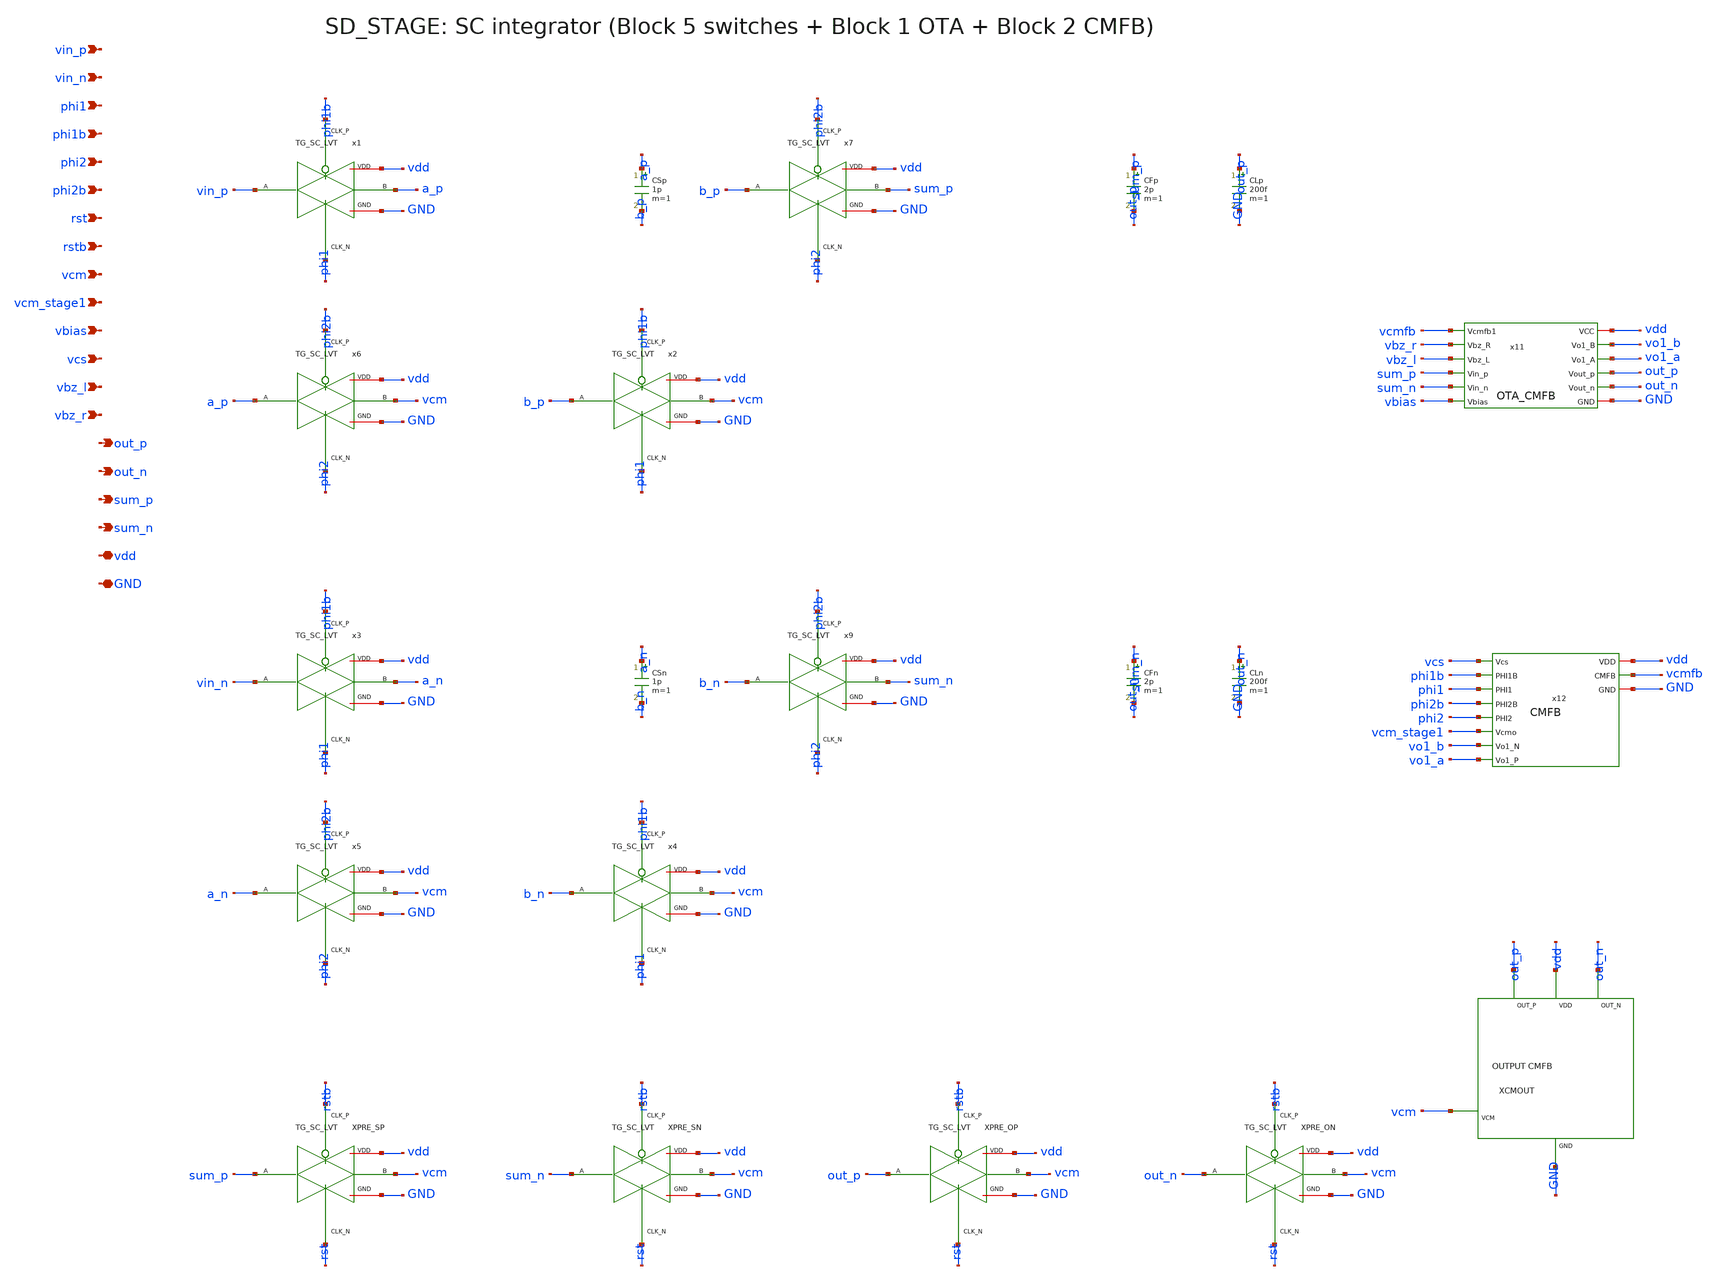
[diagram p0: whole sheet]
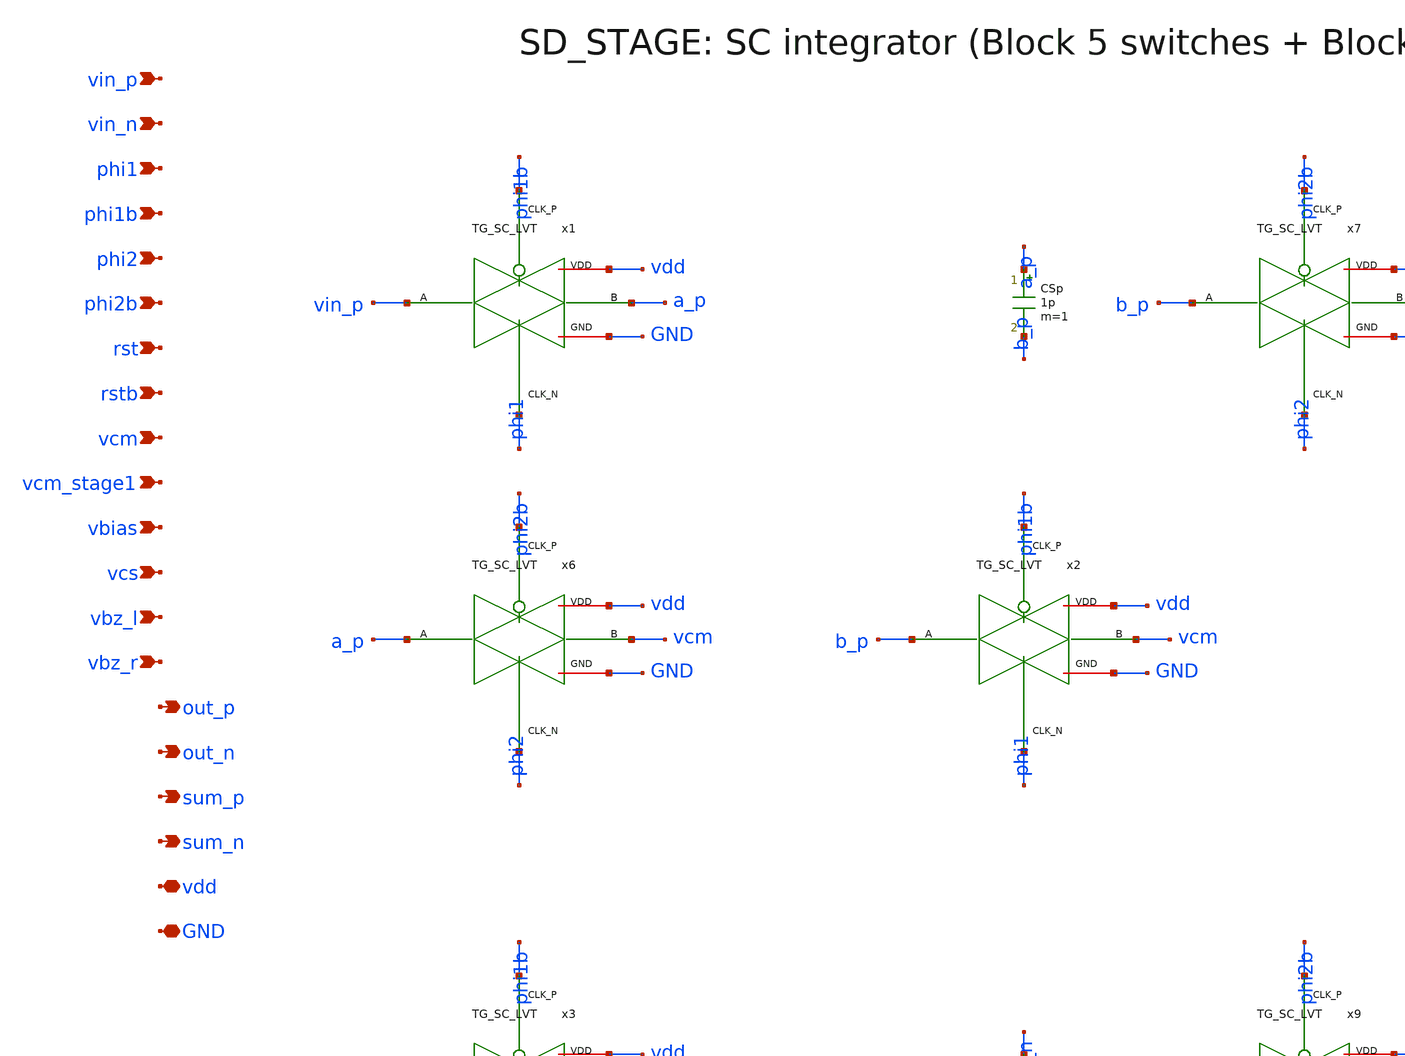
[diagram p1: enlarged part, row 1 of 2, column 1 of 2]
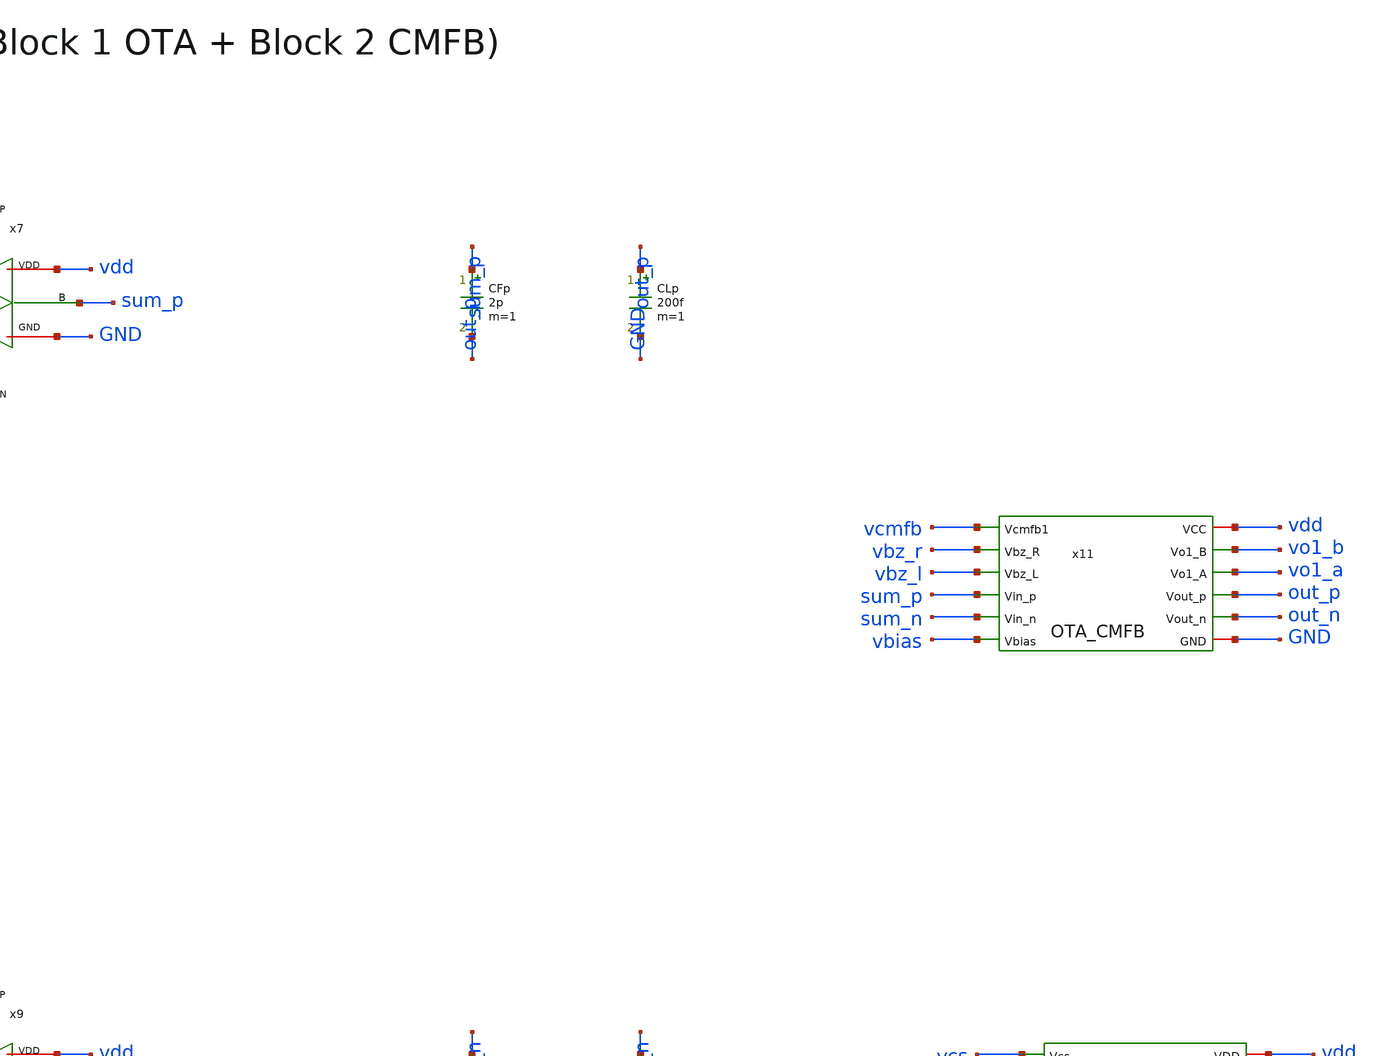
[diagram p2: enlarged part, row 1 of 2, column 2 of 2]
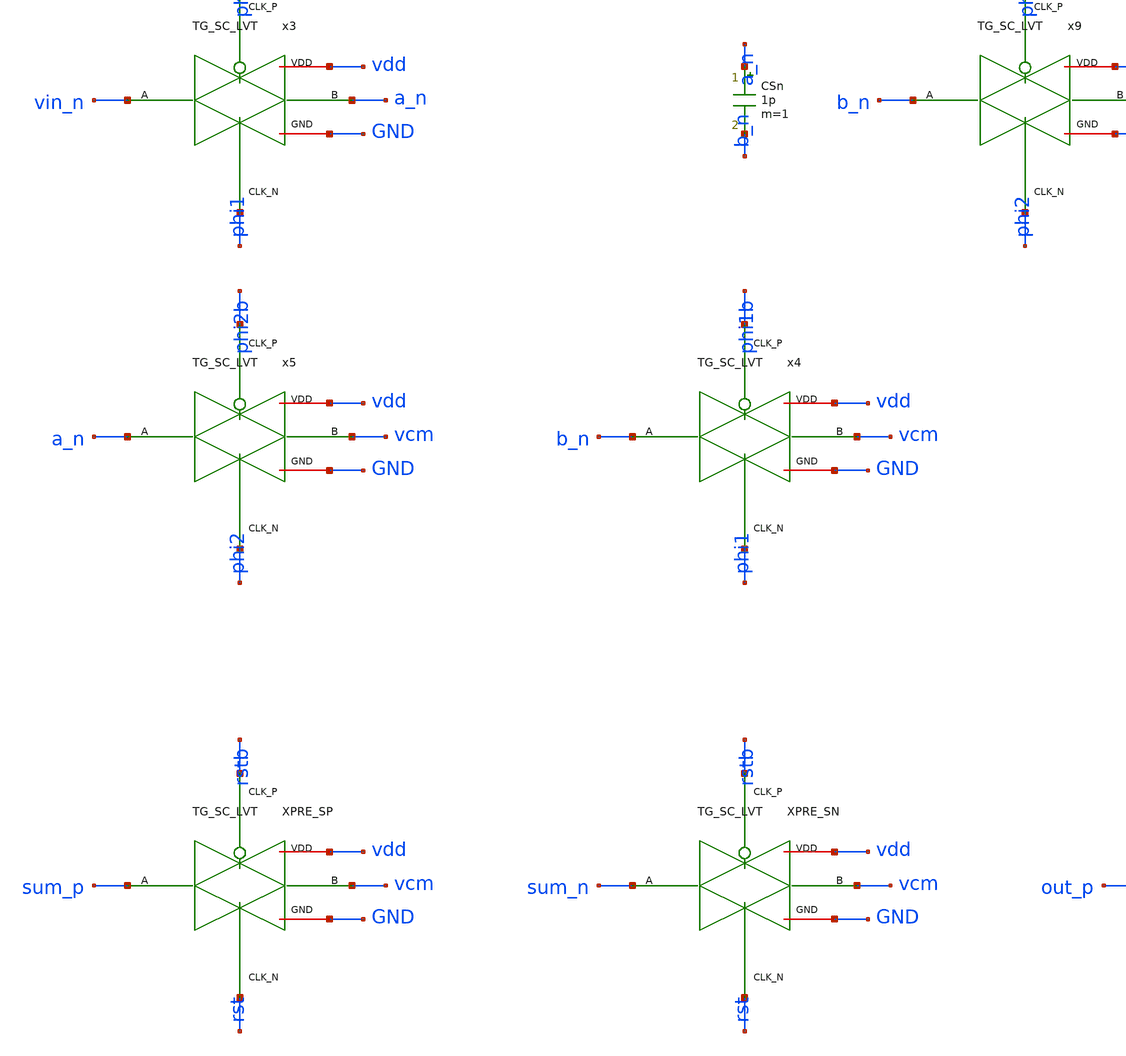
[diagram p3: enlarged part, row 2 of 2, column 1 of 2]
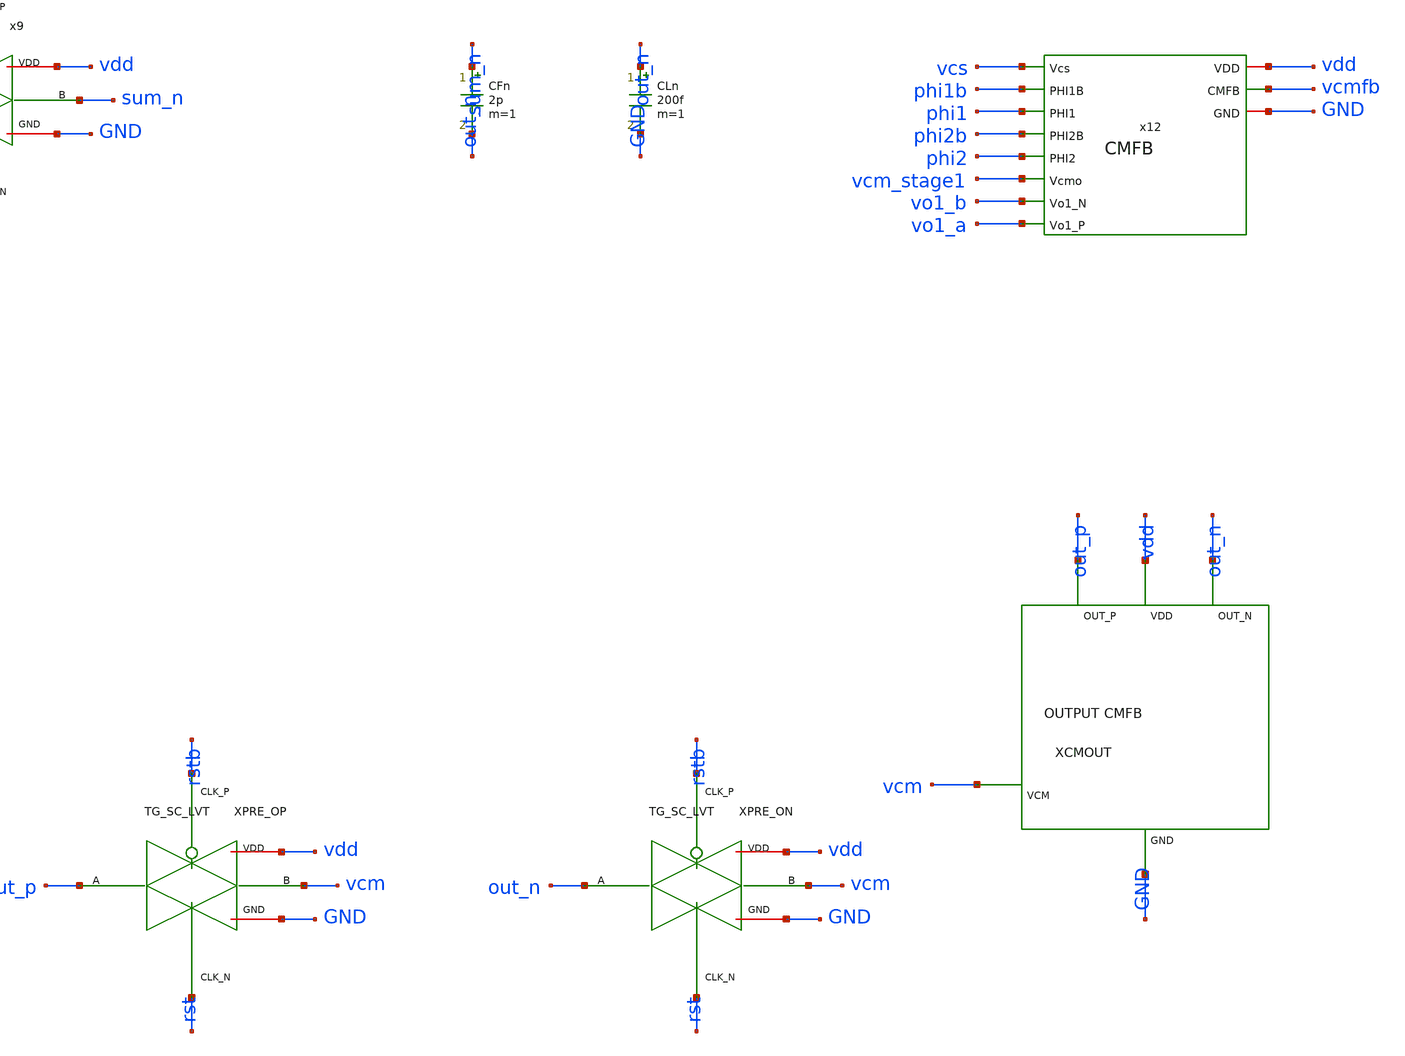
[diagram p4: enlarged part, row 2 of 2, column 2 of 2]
** sch_path: top_level/xschem/SD_STAGE.sch
**.subckt SD_STAGE vin_p vin_n phi1 phi1b phi2 phi2b rst rstb vcm vcm_stage1 vbias vcs vbz_l vbz_r
*+ out_p out_n sum_p sum_n vdd GND
*.ipin vin_p
*.ipin vin_n
*.ipin phi1
*.ipin phi1b
*.ipin phi2
*.ipin phi2b
*.ipin rst
*.ipin rstb
*.ipin vcm
*.ipin vcm_stage1
*.ipin vbias
*.ipin vcs
*.ipin vbz_l
*.ipin vbz_r
*.opin out_p
*.opin out_n
*.opin sum_p
*.opin sum_n
*.iopin vdd
*.iopin GND
x1 vin_p a_p phi1b phi1 vdd GND TG_SC_LVT
x7 b_p sum_p phi2b phi2 vdd GND TG_SC_LVT
x6 a_p vcm phi2b phi2 vdd GND TG_SC_LVT
x2 b_p vcm phi1b phi1 vdd GND TG_SC_LVT
x3 vin_n a_n phi1b phi1 vdd GND TG_SC_LVT
x9 b_n sum_n phi2b phi2 vdd GND TG_SC_LVT
x5 a_n vcm phi2b phi2 vdd GND TG_SC_LVT
x4 b_n vcm phi1b phi1 vdd GND TG_SC_LVT
XPRE_SP sum_p vcm rstb rst vdd GND TG_SC_LVT
XPRE_SN sum_n vcm rstb rst vdd GND TG_SC_LVT
XPRE_OP out_p vcm rstb rst vdd GND TG_SC_LVT
XPRE_ON out_n vcm rstb rst vdd GND TG_SC_LVT
CSp a_p b_p 1p m=1
CSn a_n b_n 1p m=1
CFp sum_p out_p 2p m=1
CLp out_p GND 200f m=1
CFn sum_n out_n 2p m=1
CLn out_n GND 200f m=1
x11 vdd vcmfb vbz_r vbz_l sum_p sum_n vo1_b vo1_a out_p out_n vbias GND OTA_CMFB
x12 vcmfb vcs phi1b phi1 vdd phi2b GND phi2 vcm_stage1 vo1_b vo1_a CMFB
XCMOUT vdd GND out_p out_n vcm CMFB_OUT_I2_Wired
**.ends
.end
